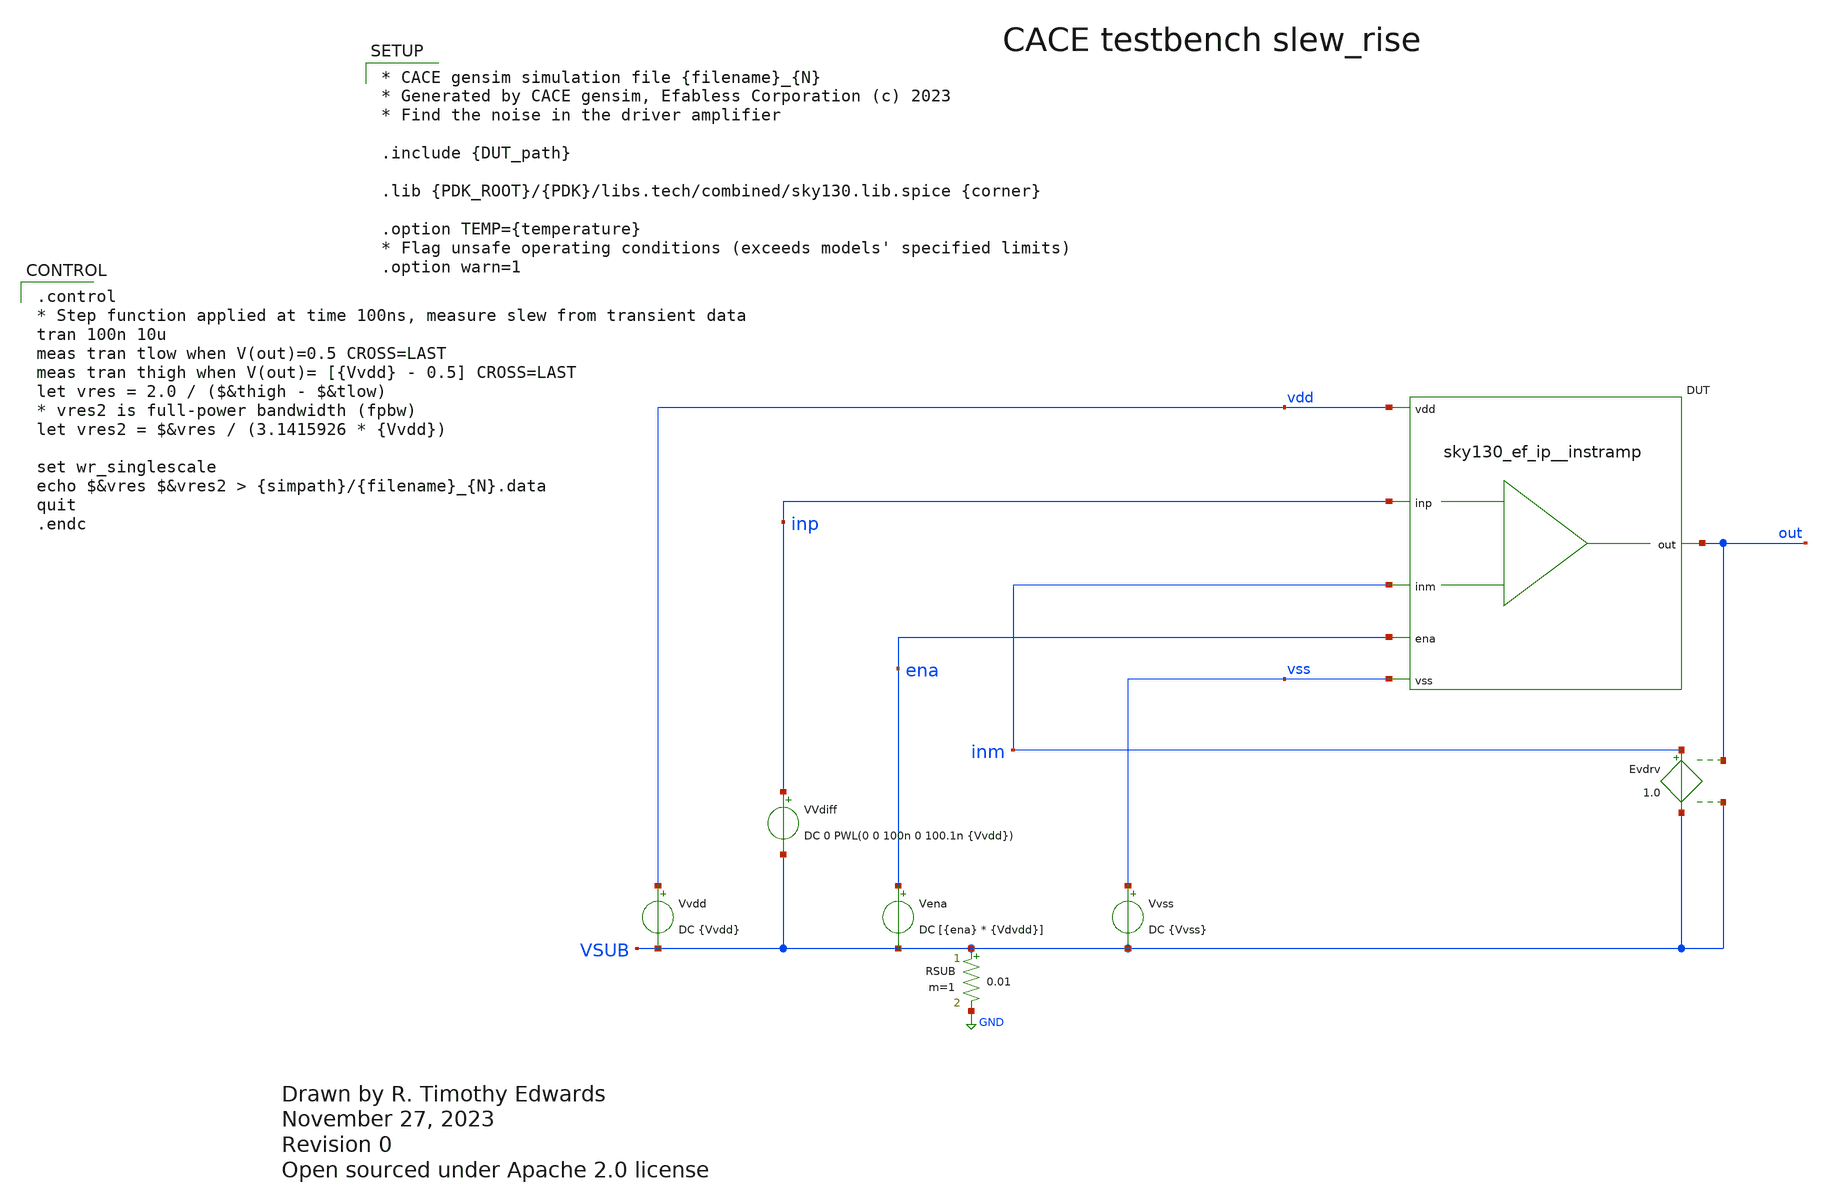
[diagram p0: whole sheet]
** sch_path: cace/slew_rise.sch
* Open sourced under Apache 2.0 license
**.subckt slew_rise
VVdiff inp VSUB DC 0 PWL(0 0 100n 0 100.1n {Vvdd})
Vena ena VSUB DC [{ena} * {Vdvdd}]
Vvss vss VSUB DC {Vvss}
Vvdd vdd VSUB DC {Vvdd}
RSUB VSUB GND 0.01 m=1
XDUT {PIN|vdd|vdd} {PIN|vss|vss} {PIN|inm|inm} {PIN|inp|inp} {PIN|out|out} {PIN|ena|ena} {DUT_name}
Evdrv inm VSUB out VSUB 1.0
**** begin user architecture code

.control
* Step function applied at time 100ns, measure slew from transient data
tran 100n 10u
meas tran tlow when V(out)=0.5 CROSS=LAST
meas tran thigh when V(out)= [{Vvdd} - 0.5] CROSS=LAST
let vres = 2.0 / ($&thigh - $&tlow)
* vres2 is full-power bandwidth (fpbw)
let vres2 = $&vres / (3.1415926 * {Vvdd})

set wr_singlescale
echo $&vres $&vres2 > {simpath}/{filename}_{N}.data
quit
.endc



* CACE gensim simulation file {filename}_{N}
* Generated by CACE gensim, Efabless Corporation (c) 2023
* Find the noise in the driver amplifier

.include {DUT_path}

.lib {PDK_ROOT}/{PDK}/libs.tech/combined/sky130.lib.spice {corner}

.option TEMP={temperature}
* Flag unsafe operating conditions (exceeds models' specified limits)
.option warn=1


**** end user architecture code
**.ends
.GLOBAL GND
.end
